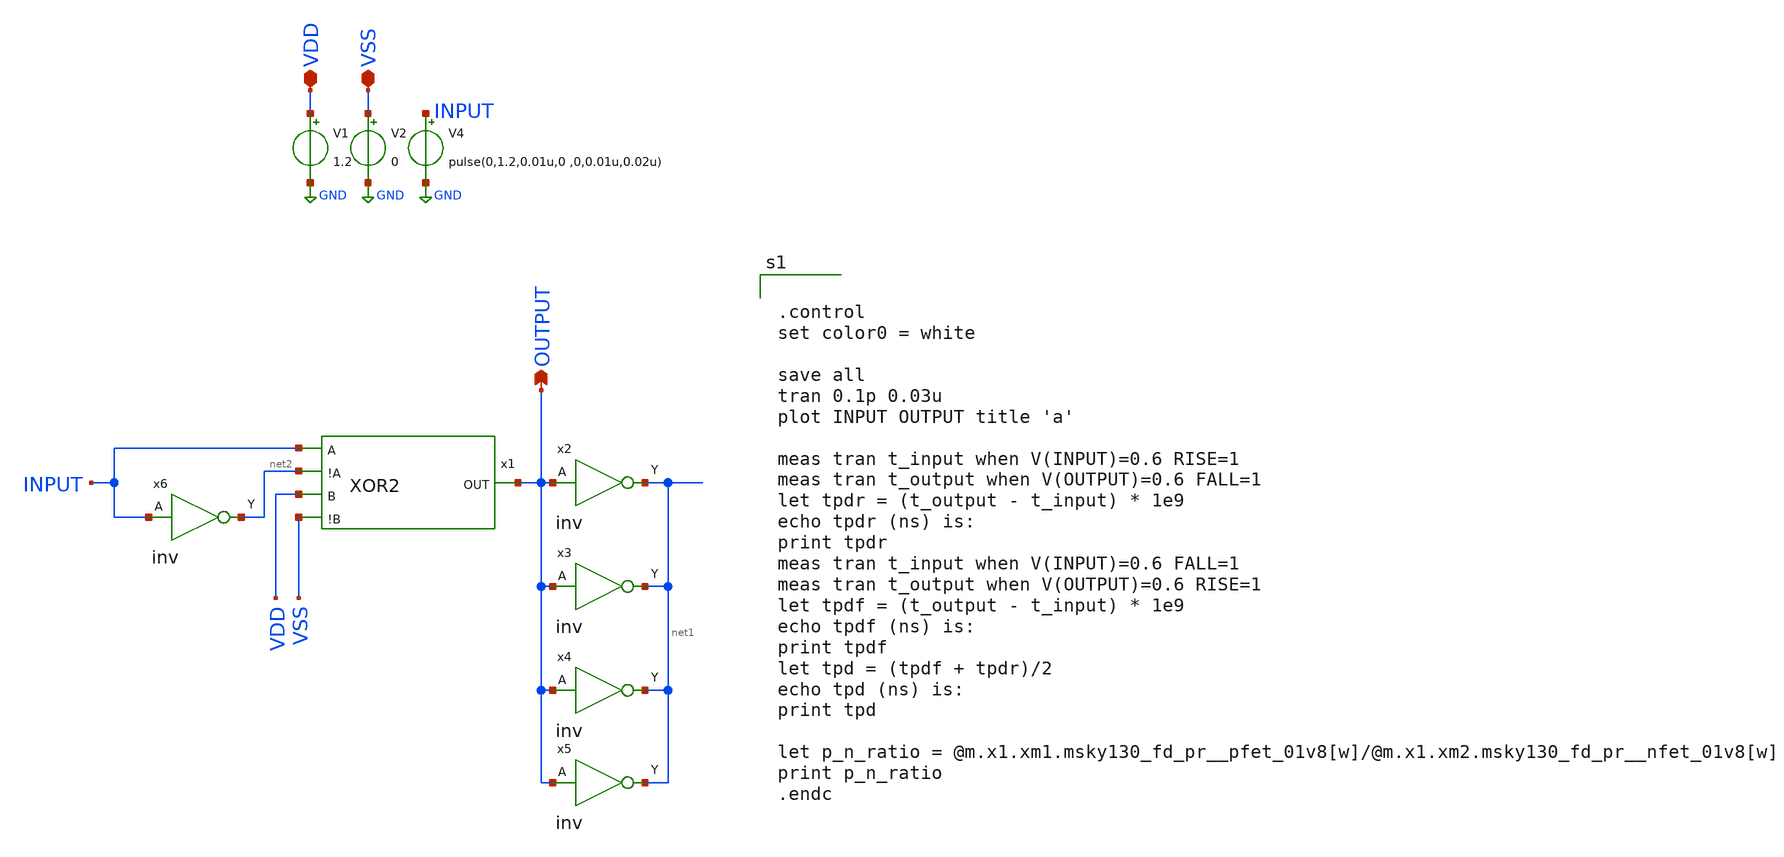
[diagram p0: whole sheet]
** sch_path: design/xschem/MUX/mux_TB.sch
**.subckt mux_TB OUTPUT VDD VSS
*.opin OUTPUT
*.iopin VDD
*.iopin VSS
V1 VDD GND 1.2
V2 VSS GND 0
V4 INPUT GND pulse(0,1.2,0.01u,0 ,0,0.01u,0.02u)
x2 OUTPUT VSS VDD net1 inv
x3 OUTPUT VSS VDD net1 inv
x4 OUTPUT VSS VDD net1 inv
x5 OUTPUT VSS VDD net1 inv
x6 INPUT VSS VDD net2 inv
x1 INPUT net2 VDD VSS OUTPUT VSS VDD XOR2
**** begin user architecture code

** opencircuitdesign pdks install
.lib $::SKYWATER_MODELS/sky130.lib.spice tt_mm




.control
set color0 = white

save all
tran 0.1p 0.03u
plot INPUT OUTPUT title 'a'

meas tran t_input when V(INPUT)=0.6 RISE=1
meas tran t_output when V(OUTPUT)=0.6 FALL=1
let tpdr = (t_output - t_input) * 1e9
echo tpdr (ns) is:
print tpdr
meas tran t_input when V(INPUT)=0.6 FALL=1
meas tran t_output when V(OUTPUT)=0.6 RISE=1
let tpdf = (t_output - t_input) * 1e9
echo tpdf (ns) is:
print tpdf
let tpd = (tpdf + tpdr)/2
echo tpd (ns) is:
print tpd

let p_n_ratio = @m.x1.xm1.msky130_fd_pr__pfet_01v8[w]/@m.x1.xm2.msky130_fd_pr__nfet_01v8[w]
print p_n_ratio
.endc


**** end user architecture code
**.ends

* expanding   symbol:  /foss/designs/xschem/INV/inv.sym # of pins=2
** sym_path: design/xschem/INV/inv.sym
** sch_path: design/xschem/INV/inv.sch
.subckt inv A VSS VDD Y
*.ipin A
*.opin Y
XM2 Y A VSS GND sky130_fd_pr__nfet_01v8 L=0.15 W=1 nf=1 ad='int((nf+1)/2) * W/nf * 0.29' as='int((nf+2)/2) * W/nf * 0.29'
+ pd='2*int((nf+1)/2) * (W/nf + 0.29)' ps='2*int((nf+2)/2) * (W/nf + 0.29)' nrd='0.29 / W' nrs='0.29 / W'
+ sa=0 sb=0 sd=0 mult=1 m=1
XM1 Y A VDD VDD sky130_fd_pr__pfet_01v8 L=0.15 W=3.21 nf=1 ad='int((nf+1)/2) * W/nf * 0.29' as='int((nf+2)/2) * W/nf * 0.29'
+ pd='2*int((nf+1)/2) * (W/nf + 0.29)' ps='2*int((nf+2)/2) * (W/nf + 0.29)' nrd='0.29 / W' nrs='0.29 / W'
+ sa=0 sb=0 sd=0 mult=1 m=1
.ends


* expanding   symbol:  /foss/designs/xschem/XOR/XOR2.sym # of pins=5
** sym_path: design/xschem/XOR/XOR2.sym
** sch_path: design/xschem/XOR/XOR2.sch
.subckt XOR2 A !A B !B OUT VSS VDD
*.ipin A
*.ipin !A
*.ipin B
*.ipin !B
*.opin OUT
x2 A B !B !A OUT !A A !B B VSS VDD cg4
.ends


* expanding   symbol:  CG4/cg4.sym # of pins=9
** sym_path: design/xschem/CG4/cg4.sym
** sch_path: design/xschem/CG4/cg4.sch
.subckt cg4 P3 P4 P2 P1 OUT N2 N1 N4 N3 VSS VDD
*.ipin P3
*.ipin P1
*.ipin N1
*.ipin N3
*.ipin P4
*.ipin P2
*.ipin N2
*.ipin N4
*.opin OUT
XM1 OUT N1 net1 VSS sky130_fd_pr__nfet_01v8 L=0.15 W=2 nf=1 ad='int((nf+1)/2) * W/nf * 0.29' as='int((nf+2)/2) * W/nf * 0.29'
+ pd='2*int((nf+1)/2) * (W/nf + 0.29)' ps='2*int((nf+2)/2) * (W/nf + 0.29)' nrd='0.29 / W' nrs='0.29 / W'
+ sa=0 sb=0 sd=0 mult=1 m=1
XM2 OUT N2 net2 VSS sky130_fd_pr__nfet_01v8 L=0.15 W=2 nf=1 ad='int((nf+1)/2) * W/nf * 0.29' as='int((nf+2)/2) * W/nf * 0.29'
+ pd='2*int((nf+1)/2) * (W/nf + 0.29)' ps='2*int((nf+2)/2) * (W/nf + 0.29)' nrd='0.29 / W' nrs='0.29 / W'
+ sa=0 sb=0 sd=0 mult=1 m=1
XM3 net1 N3 VSS VSS sky130_fd_pr__nfet_01v8 L=0.15 W=2 nf=1 ad='int((nf+1)/2) * W/nf * 0.29' as='int((nf+2)/2) * W/nf * 0.29'
+ pd='2*int((nf+1)/2) * (W/nf + 0.29)' ps='2*int((nf+2)/2) * (W/nf + 0.29)' nrd='0.29 / W' nrs='0.29 / W'
+ sa=0 sb=0 sd=0 mult=1 m=1
XM4 net2 N4 VSS VSS sky130_fd_pr__nfet_01v8 L=0.15 W=2 nf=1 ad='int((nf+1)/2) * W/nf * 0.29' as='int((nf+2)/2) * W/nf * 0.29'
+ pd='2*int((nf+1)/2) * (W/nf + 0.29)' ps='2*int((nf+2)/2) * (W/nf + 0.29)' nrd='0.29 / W' nrs='0.29 / W'
+ sa=0 sb=0 sd=0 mult=1 m=1
XM5 OUT P1 net3 VDD sky130_fd_pr__pfet_01v8 L=0.15 W=8.25 nf=1 ad='int((nf+1)/2) * W/nf * 0.29' as='int((nf+2)/2) * W/nf * 0.29'
+ pd='2*int((nf+1)/2) * (W/nf + 0.29)' ps='2*int((nf+2)/2) * (W/nf + 0.29)' nrd='0.29 / W' nrs='0.29 / W'
+ sa=0 sb=0 sd=0 mult=1 m=1
XM6 OUT P2 net3 VDD sky130_fd_pr__pfet_01v8 L=0.15 W=8.25 nf=1 ad='int((nf+1)/2) * W/nf * 0.29' as='int((nf+2)/2) * W/nf * 0.29'
+ pd='2*int((nf+1)/2) * (W/nf + 0.29)' ps='2*int((nf+2)/2) * (W/nf + 0.29)' nrd='0.29 / W' nrs='0.29 / W'
+ sa=0 sb=0 sd=0 mult=1 m=1
XM7 net3 P3 VDD VDD sky130_fd_pr__pfet_01v8 L=0.15 W=8.25 nf=1 ad='int((nf+1)/2) * W/nf * 0.29' as='int((nf+2)/2) * W/nf * 0.29'
+ pd='2*int((nf+1)/2) * (W/nf + 0.29)' ps='2*int((nf+2)/2) * (W/nf + 0.29)' nrd='0.29 / W' nrs='0.29 / W'
+ sa=0 sb=0 sd=0 mult=1 m=1
XM8 net3 P4 VDD VDD sky130_fd_pr__pfet_01v8 L=0.15 W=8.25 nf=1 ad='int((nf+1)/2) * W/nf * 0.29' as='int((nf+2)/2) * W/nf * 0.29'
+ pd='2*int((nf+1)/2) * (W/nf + 0.29)' ps='2*int((nf+2)/2) * (W/nf + 0.29)' nrd='0.29 / W' nrs='0.29 / W'
+ sa=0 sb=0 sd=0 mult=1 m=1
.ends

.GLOBAL GND
.end
